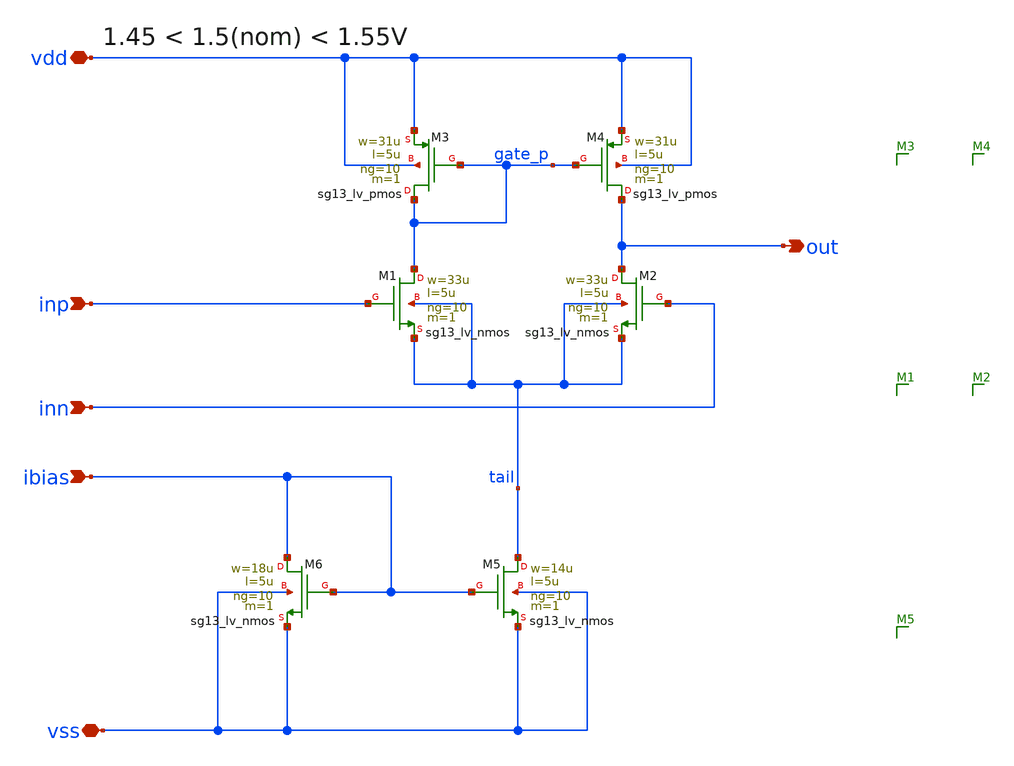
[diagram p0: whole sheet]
** sch_path: prj/template/3_Real_circuits/ota_gm_100u_se.sch
* (c) 2024-2025 M. Meiners, Apache-2.0 license
**.subckt ota_gm_100u_se ibias vdd vss inp inn out
*.ipin ibias
*.iopin vdd
*.iopin vss
*.ipin inp
*.ipin inn
*.opin out
XM5 tail ibias vss vss sg13_lv_nmos w=14u l=5u ng=10 m=1 mm_ok=1
XM4 out gate_p vdd vdd sg13_lv_pmos w=31u l=5u ng=10 m=1 mm_ok=1
XM1 gate_p inp tail tail sg13_lv_nmos w=33u l=5u ng=10 m=1 mm_ok=1
XM2 out inn tail tail sg13_lv_nmos w=33u l=5u ng=10 m=1 mm_ok=1
XM3 gate_p gate_p vdd vdd sg13_lv_pmos w=31u l=5u ng=10 m=1 mm_ok=1
XM6 ibias ibias vss vss sg13_lv_nmos w=18u l=5u ng=10 m=1 mm_ok=1
**.ends
.end
